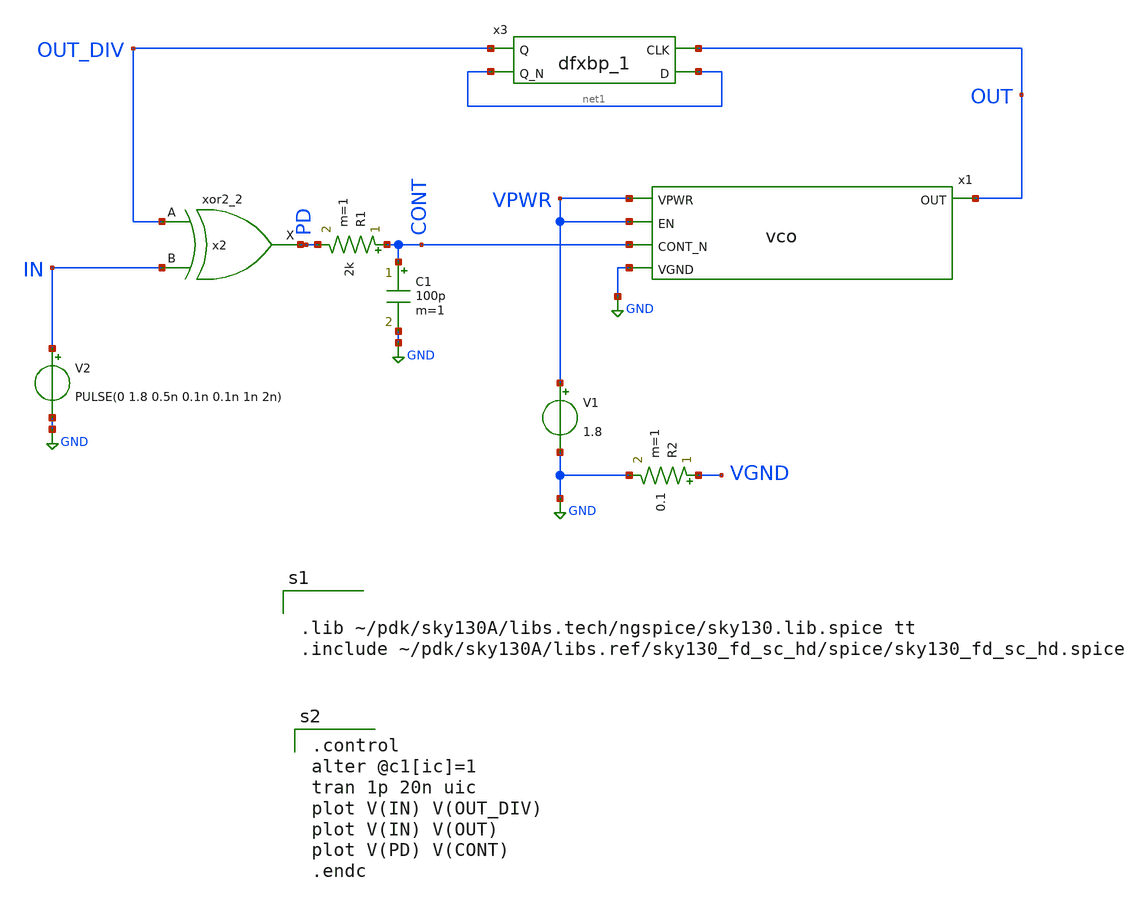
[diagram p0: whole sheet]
** sch_path: xschem/ring_osc/pfd_pll.sch
**.subckt pfd_pll
x1 VPWR VPWR OUT CONT GND vco
R1 CONT PD 2k m=1
C1 CONT GND 100p m=1
x2 OUT_DIV IN VGND VNB VPB VPWR PD sky130_fd_sc_hd__xor2_2
V1 VPWR GND 1.8
V2 IN GND PULSE(0 1.8 0.5n 0.1n 0.1n 1n 2n)
R2 VGND GND 0.1 m=1
x3 OUT net1 VGND VNB VPB VPWR OUT_DIV net1 sky130_fd_sc_hd__dfxbp_1
**** begin user architecture code


.lib ~/pdk/sky130A/libs.tech/ngspice/sky130.lib.spice tt
.include ~/pdk/sky130A/libs.ref/sky130_fd_sc_hd/spice/sky130_fd_sc_hd.spice



.control
alter @c1[ic]=1
tran 1p 20n uic
plot V(IN) V(OUT_DIV)
plot V(IN) V(OUT)
plot V(PD) V(CONT)
.endc

**** end user architecture code
**.ends

* expanding   symbol:  vco.sym # of pins=5
** sym_path: xschem/ring_osc/vco.sym
** sch_path: xschem/ring_osc/vco.sch
.subckt vco EN VPWR OUT CONT_N VGND
*.ipin CONT_N
*.ipin VGND
*.ipin VPWR
*.ipin EN
*.opin OUT
x1 VPWR CONT_P net2 MID CONT_N VGND delay_cell
XM1 CONT_P CONT_N VGND VGND sky130_fd_pr__nfet_01v8 L=0.15 W=1 nf=1 ad='int((nf+1)/2) * W/nf * 0.29'
+ as='int((nf+2)/2) * W/nf * 0.29' pd='2*int((nf+1)/2) * (W/nf + 0.29)' ps='2*int((nf+2)/2) * (W/nf + 0.29)'
+ nrd='0.29 / W' nrs='0.29 / W' sa=0 sb=0 sd=0 mult=1 m=1
XM2 CONT_P CONT_P VPWR VPWR sky130_fd_pr__pfet_01v8 L=0.15 W=1.5 nf=1 ad='int((nf+1)/2) * W/nf * 0.29'
+ as='int((nf+2)/2) * W/nf * 0.29' pd='2*int((nf+1)/2) * (W/nf + 0.29)' ps='2*int((nf+2)/2) * (W/nf + 0.29)'
+ nrd='0.29 / W' nrs='0.29 / W' sa=0 sb=0 sd=0 mult=1 m=1
x2 VPWR CONT_P MID net3 CONT_N VGND delay_cell
x3 VPWR CONT_P net1 net2 CONT_N VGND delay_cell
x5 VPWR CONT_P net3 net5 CONT_N VGND delay_cell
XM3 OUT net1 VGND VGND sky130_fd_pr__nfet_01v8 L=0.15 W=1 nf=1 ad='int((nf+1)/2) * W/nf * 0.29' as='int((nf+2)/2) * W/nf * 0.29'
+ pd='2*int((nf+1)/2) * (W/nf + 0.29)' ps='2*int((nf+2)/2) * (W/nf + 0.29)' nrd='0.29 / W' nrs='0.29 / W'
+ sa=0 sb=0 sd=0 mult=1 m=1
XM4 OUT net1 VPWR VPWR sky130_fd_pr__pfet_01v8 L=0.15 W=1.5 nf=1 ad='int((nf+1)/2) * W/nf * 0.29' as='int((nf+2)/2) * W/nf * 0.29'
+ pd='2*int((nf+1)/2) * (W/nf + 0.29)' ps='2*int((nf+2)/2) * (W/nf + 0.29)' nrd='0.29 / W' nrs='0.29 / W'
+ sa=0 sb=0 sd=0 mult=1 m=1
XM6 net1 EN net4 VGND sky130_fd_pr__nfet_01v8 L=0.15 W=1 nf=1 ad='int((nf+1)/2) * W/nf * 0.29' as='int((nf+2)/2) * W/nf * 0.29'
+ pd='2*int((nf+1)/2) * (W/nf + 0.29)' ps='2*int((nf+2)/2) * (W/nf + 0.29)' nrd='0.29 / W' nrs='0.29 / W'
+ sa=0 sb=0 sd=0 mult=1 m=1
XM7 net1 net5 VPWR VPWR sky130_fd_pr__pfet_01v8 L=0.15 W=1.5 nf=1 ad='int((nf+1)/2) * W/nf * 0.29' as='int((nf+2)/2) * W/nf * 0.29'
+ pd='2*int((nf+1)/2) * (W/nf + 0.29)' ps='2*int((nf+2)/2) * (W/nf + 0.29)' nrd='0.29 / W' nrs='0.29 / W'
+ sa=0 sb=0 sd=0 mult=1 m=1
XM8 net4 net5 VGND VGND sky130_fd_pr__nfet_01v8 L=0.15 W=1 nf=1 ad='int((nf+1)/2) * W/nf * 0.29' as='int((nf+2)/2) * W/nf * 0.29'
+ pd='2*int((nf+1)/2) * (W/nf + 0.29)' ps='2*int((nf+2)/2) * (W/nf + 0.29)' nrd='0.29 / W' nrs='0.29 / W'
+ sa=0 sb=0 sd=0 mult=1 m=1
XM5 net1 EN VPWR VPWR sky130_fd_pr__pfet_01v8 L=0.15 W=1.5 nf=1 ad='int((nf+1)/2) * W/nf * 0.29' as='int((nf+2)/2) * W/nf * 0.29'
+ pd='2*int((nf+1)/2) * (W/nf + 0.29)' ps='2*int((nf+2)/2) * (W/nf + 0.29)' nrd='0.29 / W' nrs='0.29 / W'
+ sa=0 sb=0 sd=0 mult=1 m=1
.ends


* expanding   symbol:  delay_cell.sym # of pins=6
** sym_path: delay_cell.sym
** sch_path: delay_cell.sch
.subckt delay_cell VPWR CONT_P IN OUT CONT_N VGND
*.ipin VPWR
*.ipin VGND
*.ipin IN
*.ipin CONT_N
*.ipin CONT_P
*.opin OUT
XM1 OUT IN net1 VGND sky130_fd_pr__nfet_01v8 L=0.15 W=1 nf=1 ad='int((nf+1)/2) * W/nf * 0.29' as='int((nf+2)/2) * W/nf * 0.29'
+ pd='2*int((nf+1)/2) * (W/nf + 0.29)' ps='2*int((nf+2)/2) * (W/nf + 0.29)' nrd='0.29 / W' nrs='0.29 / W'
+ sa=0 sb=0 sd=0 mult=1 m=1
XM2 net1 CONT_N VGND VGND sky130_fd_pr__nfet_01v8 L=0.15 W=1 nf=1 ad='int((nf+1)/2) * W/nf * 0.29' as='int((nf+2)/2) * W/nf * 0.29'
+ pd='2*int((nf+1)/2) * (W/nf + 0.29)' ps='2*int((nf+2)/2) * (W/nf + 0.29)' nrd='0.29 / W' nrs='0.29 / W'
+ sa=0 sb=0 sd=0 mult=1 m=1
XM3 OUT IN net2 VPWR sky130_fd_pr__pfet_01v8 L=0.15 W=1 nf=1 ad='int((nf+1)/2) * W/nf * 0.29' as='int((nf+2)/2) * W/nf * 0.29'
+ pd='2*int((nf+1)/2) * (W/nf + 0.29)' ps='2*int((nf+2)/2) * (W/nf + 0.29)' nrd='0.29 / W' nrs='0.29 / W'
+ sa=0 sb=0 sd=0 mult=1 m=1
XM4 net2 CONT_P VPWR VPWR sky130_fd_pr__pfet_01v8 L=0.15 W=1.5 nf=1 ad='int((nf+1)/2) * W/nf * 0.29'
+ as='int((nf+2)/2) * W/nf * 0.29' pd='2*int((nf+1)/2) * (W/nf + 0.29)' ps='2*int((nf+2)/2) * (W/nf + 0.29)'
+ nrd='0.29 / W' nrs='0.29 / W' sa=0 sb=0 sd=0 mult=1 m=1
.ends

.GLOBAL GND
.end
